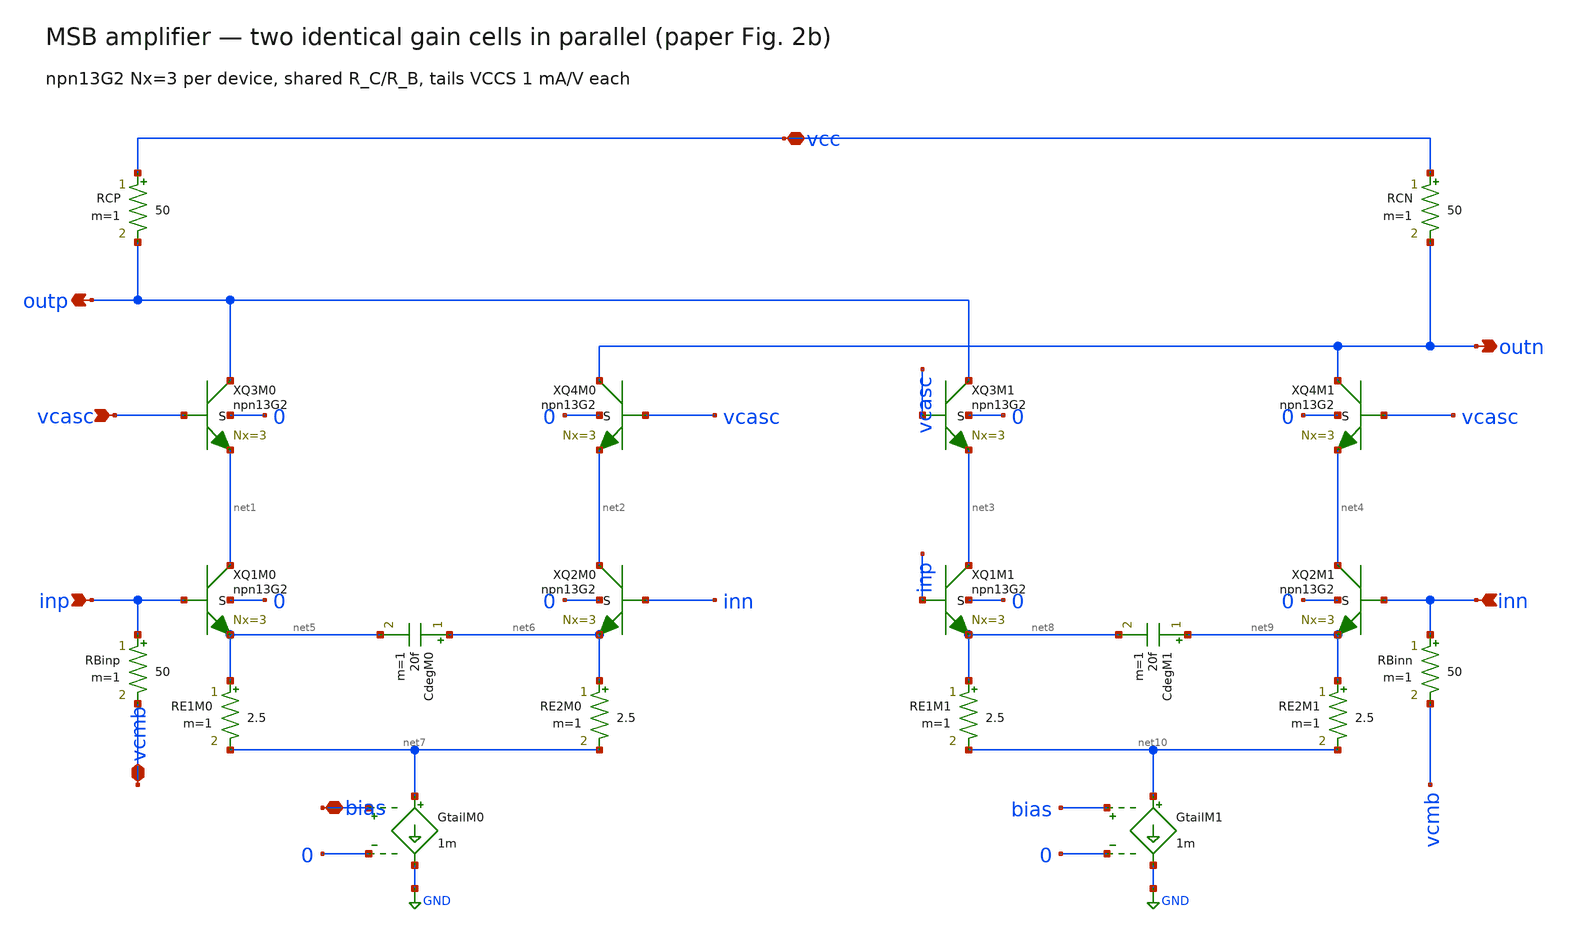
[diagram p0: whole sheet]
** sch_path: analog-db/drawings/pam4-driver-2-bit-dac-HBT/ported-netlists/schematics/dut_msb.sch
**.subckt dut_msb vcc outp outn vcasc inp inn bias vcmb
*.iopin vcc
*.opin outp
*.opin outn
*.ipin vcasc
*.ipin inp
*.ipin inn
*.iopin bias
*.iopin vcmb
RCP vcc outp 50 m=1
RCN vcc outn 50 m=1
XQ3M0 outp vcasc net1 0 npn13G2 Nx=3
XQ4M0 outn vcasc net2 0 npn13G2 Nx=3
XQ1M0 net1 inp net5 0 npn13G2 Nx=3
XQ2M0 net2 inn net6 0 npn13G2 Nx=3
XQ3M1 outp vcasc net3 0 npn13G2 Nx=3
XQ4M1 outn vcasc net4 0 npn13G2 Nx=3
XQ1M1 net3 inp net8 0 npn13G2 Nx=3
XQ2M1 net4 inn net9 0 npn13G2 Nx=3
CdegM0 net6 net5 20f m=1
RE1M0 net5 net7 2.5 m=1
RE2M0 net6 net7 2.5 m=1
GtailM0 net7 GND bias 0 1m
CdegM1 net9 net8 20f m=1
RE1M1 net8 net10 2.5 m=1
RE2M1 net9 net10 2.5 m=1
GtailM1 net10 GND bias 0 1m
RBinp inp vcmb 50 m=1
RBinn inn vcmb 50 m=1
**.ends
.GLOBAL GND
.end
